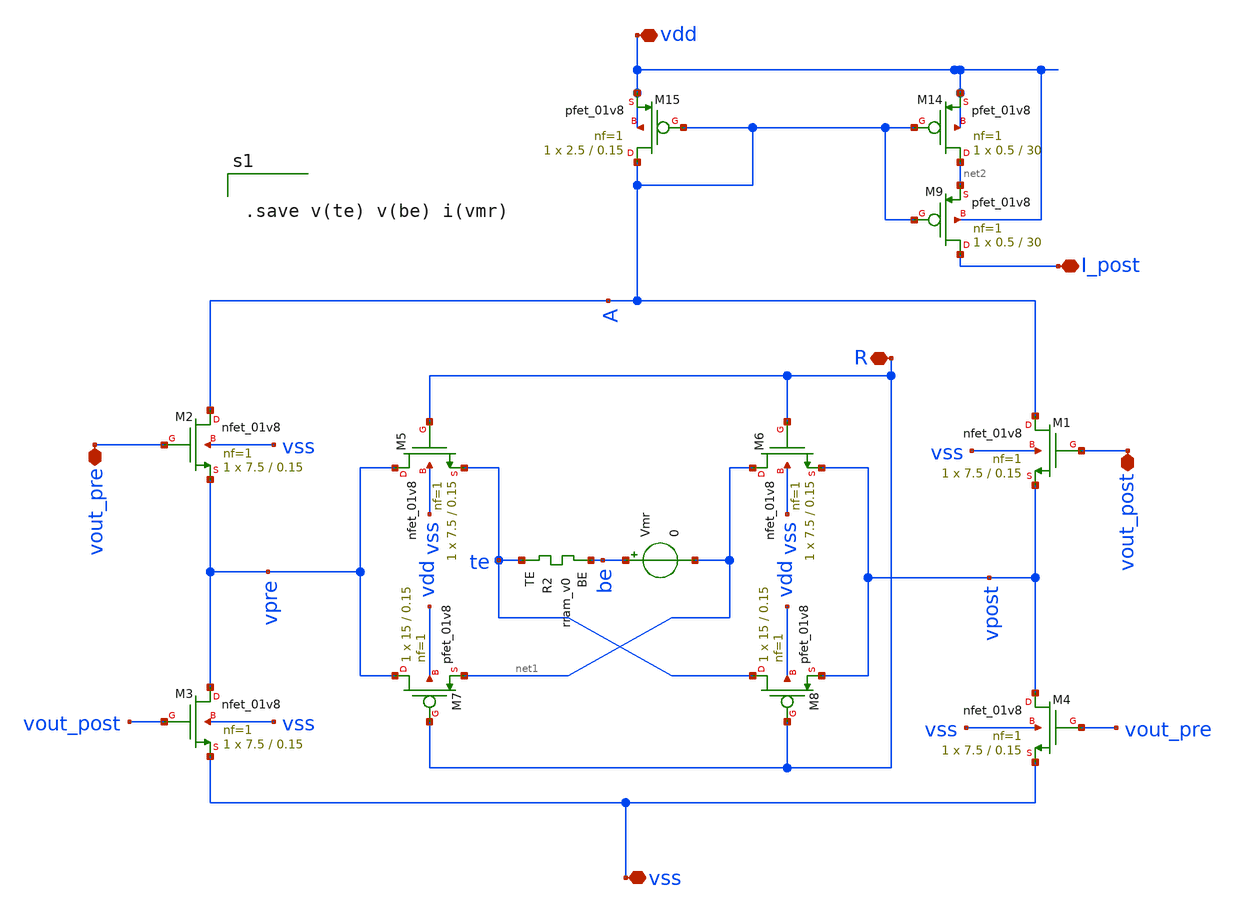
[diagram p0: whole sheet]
** sch_path: Synapse/rstdp_mirror.sch
**.subckt rstdp_mirror vdd vss R vout_post vout_pre I_post
*.iopin vdd
*.iopin vss
*.iopin R
*.iopin vout_post
*.iopin vout_pre
*.iopin I_post
XM2 A vout_pre vpre vss sky130_fd_pr__nfet_01v8 L=0.15 W=7.5 nf=1 ad='int((nf+1)/2) * W/nf * 0.29' as='int((nf+2)/2) * W/nf * 0.29'
+ pd='2*int((nf+1)/2) * (W/nf + 0.29)' ps='2*int((nf+2)/2) * (W/nf + 0.29)' nrd='0.29 / W' nrs='0.29 / W'
+ sa=0 sb=0 sd=0 mult=1 m=1
XM3 vpre vout_post vss vss sky130_fd_pr__nfet_01v8 L=0.15 W=7.5 nf=1 ad='int((nf+1)/2) * W/nf * 0.29'
+ as='int((nf+2)/2) * W/nf * 0.29' pd='2*int((nf+1)/2) * (W/nf + 0.29)' ps='2*int((nf+2)/2) * (W/nf + 0.29)'
+ nrd='0.29 / W' nrs='0.29 / W' sa=0 sb=0 sd=0 mult=1 m=1
XM1 A vout_post vpost vss sky130_fd_pr__nfet_01v8 L=0.15 W=7.5 nf=1 ad='int((nf+1)/2) * W/nf * 0.29'
+ as='int((nf+2)/2) * W/nf * 0.29' pd='2*int((nf+1)/2) * (W/nf + 0.29)' ps='2*int((nf+2)/2) * (W/nf + 0.29)'
+ nrd='0.29 / W' nrs='0.29 / W' sa=0 sb=0 sd=0 mult=1 m=1
XM4 vpost vout_pre vss vss sky130_fd_pr__nfet_01v8 L=0.15 W=7.5 nf=1 ad='int((nf+1)/2) * W/nf * 0.29'
+ as='int((nf+2)/2) * W/nf * 0.29' pd='2*int((nf+1)/2) * (W/nf + 0.29)' ps='2*int((nf+2)/2) * (W/nf + 0.29)'
+ nrd='0.29 / W' nrs='0.29 / W' sa=0 sb=0 sd=0 mult=1 m=1
XR2 te be rram_v0
XM5 vpre R te vss sky130_fd_pr__nfet_01v8 L=0.15 W=7.5 nf=1 ad='int((nf+1)/2) * W/nf * 0.29' as='int((nf+2)/2) * W/nf * 0.29'
+ pd='2*int((nf+1)/2) * (W/nf + 0.29)' ps='2*int((nf+2)/2) * (W/nf + 0.29)' nrd='0.29 / W' nrs='0.29 / W'
+ sa=0 sb=0 sd=0 mult=1 m=1
XM6 net1 R vpost vss sky130_fd_pr__nfet_01v8 L=0.15 W=7.5 nf=1 ad='int((nf+1)/2) * W/nf * 0.29' as='int((nf+2)/2) * W/nf * 0.29'
+ pd='2*int((nf+1)/2) * (W/nf + 0.29)' ps='2*int((nf+2)/2) * (W/nf + 0.29)' nrd='0.29 / W' nrs='0.29 / W'
+ sa=0 sb=0 sd=0 mult=1 m=1
XM7 vpre R net1 vdd sky130_fd_pr__pfet_01v8 L=0.15 W=15 nf=1 ad='int((nf+1)/2) * W/nf * 0.29' as='int((nf+2)/2) * W/nf * 0.29'
+ pd='2*int((nf+1)/2) * (W/nf + 0.29)' ps='2*int((nf+2)/2) * (W/nf + 0.29)' nrd='0.29 / W' nrs='0.29 / W'
+ sa=0 sb=0 sd=0 mult=1 m=1
XM8 te R vpost vdd sky130_fd_pr__pfet_01v8 L=0.15 W=15 nf=1 ad='int((nf+1)/2) * W/nf * 0.29' as='int((nf+2)/2) * W/nf * 0.29'
+ pd='2*int((nf+1)/2) * (W/nf + 0.29)' ps='2*int((nf+2)/2) * (W/nf + 0.29)' nrd='0.29 / W' nrs='0.29 / W'
+ sa=0 sb=0 sd=0 mult=1 m=1
XM14 net2 A vdd vdd sky130_fd_pr__pfet_01v8 L=30 W=0.5 nf=1 ad='int((nf+1)/2) * W/nf * 0.29' as='int((nf+2)/2) * W/nf * 0.29'
+ pd='2*int((nf+1)/2) * (W/nf + 0.29)' ps='2*int((nf+2)/2) * (W/nf + 0.29)' nrd='0.29 / W' nrs='0.29 / W'
+ sa=0 sb=0 sd=0 mult=1 m=1
XM15 A A vdd vdd sky130_fd_pr__pfet_01v8 L=0.15 W=2.5 nf=1 ad='int((nf+1)/2) * W/nf * 0.29' as='int((nf+2)/2) * W/nf * 0.29'
+ pd='2*int((nf+1)/2) * (W/nf + 0.29)' ps='2*int((nf+2)/2) * (W/nf + 0.29)' nrd='0.29 / W' nrs='0.29 / W'
+ sa=0 sb=0 sd=0 mult=1 m=1
Vmr be net1 0
.save i(vmr)
XM9 I_post A net2 vdd sky130_fd_pr__pfet_01v8 L=30 W=0.5 nf=1 ad='int((nf+1)/2) * W/nf * 0.29' as='int((nf+2)/2) * W/nf * 0.29'
+ pd='2*int((nf+1)/2) * (W/nf + 0.29)' ps='2*int((nf+2)/2) * (W/nf + 0.29)' nrd='0.29 / W' nrs='0.29 / W'
+ sa=0 sb=0 sd=0 mult=1 m=1
**** begin user architecture code


.save v(te) v(be) i(vmr)


**** end user architecture code
**.ends
.end
